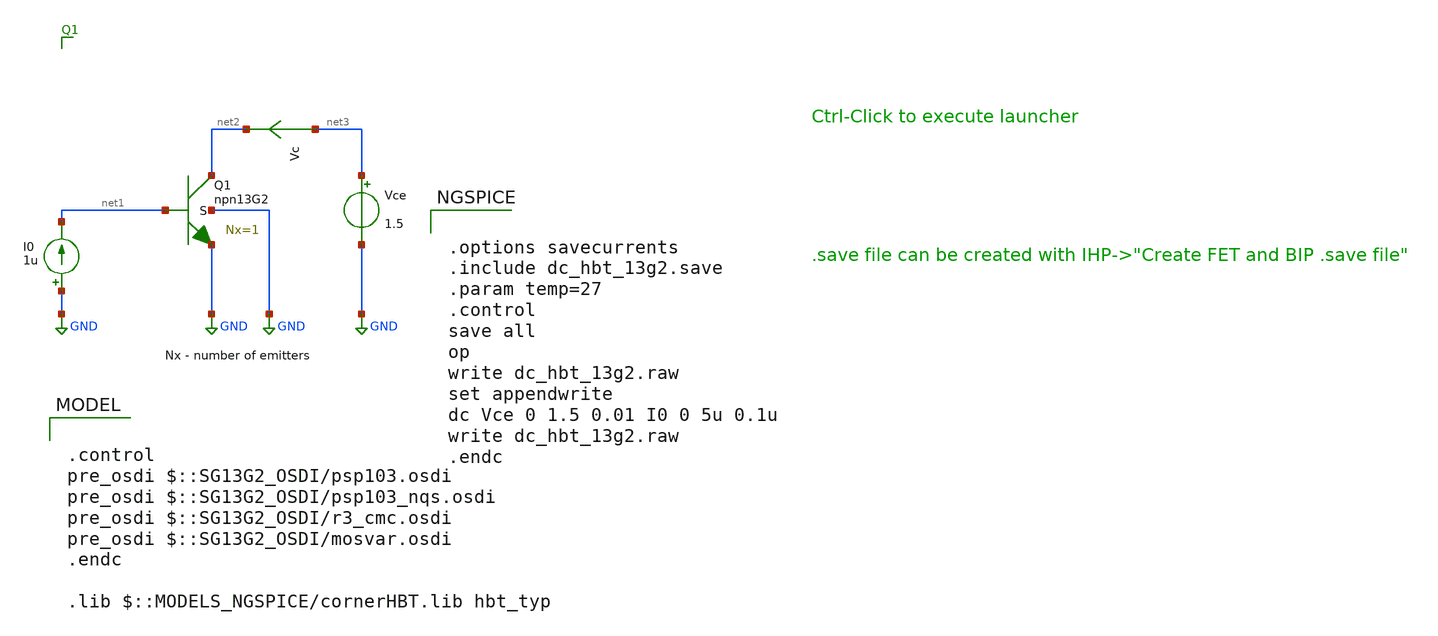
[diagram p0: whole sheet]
** sch_path: ihp-sg13g2/xschem_libs/sg13g2_tests/dc_hbt_13g2/schematic/dc_hbt_13g2.sch
* Copyright 2023 IHP PDK Authors
**.subckt dc_hbt_13g2
Vce net3 GND 1.5
I0 GND net1 1u
Vc net3 net2 0
.save i(vc)
XQ1 net2 net1 GND GND npn13G2 Nx=1 mm_ok=1
**** begin user architecture code

.control
pre_osdi $::SG13G2_OSDI/psp103.osdi
pre_osdi $::SG13G2_OSDI/psp103_nqs.osdi
pre_osdi $::SG13G2_OSDI/r3_cmc.osdi
pre_osdi $::SG13G2_OSDI/mosvar.osdi
.endc

.lib $::MODELS_NGSPICE/cornerHBT.lib hbt_typ



.options savecurrents
.include dc_hbt_13g2.save
.param temp=27
.control
save all
op
write dc_hbt_13g2.raw
set appendwrite
dc Vce 0 1.5 0.01 I0 0 5u 0.1u
write dc_hbt_13g2.raw
.endc


**** end user architecture code
**.ends
.GLOBAL GND
.end
